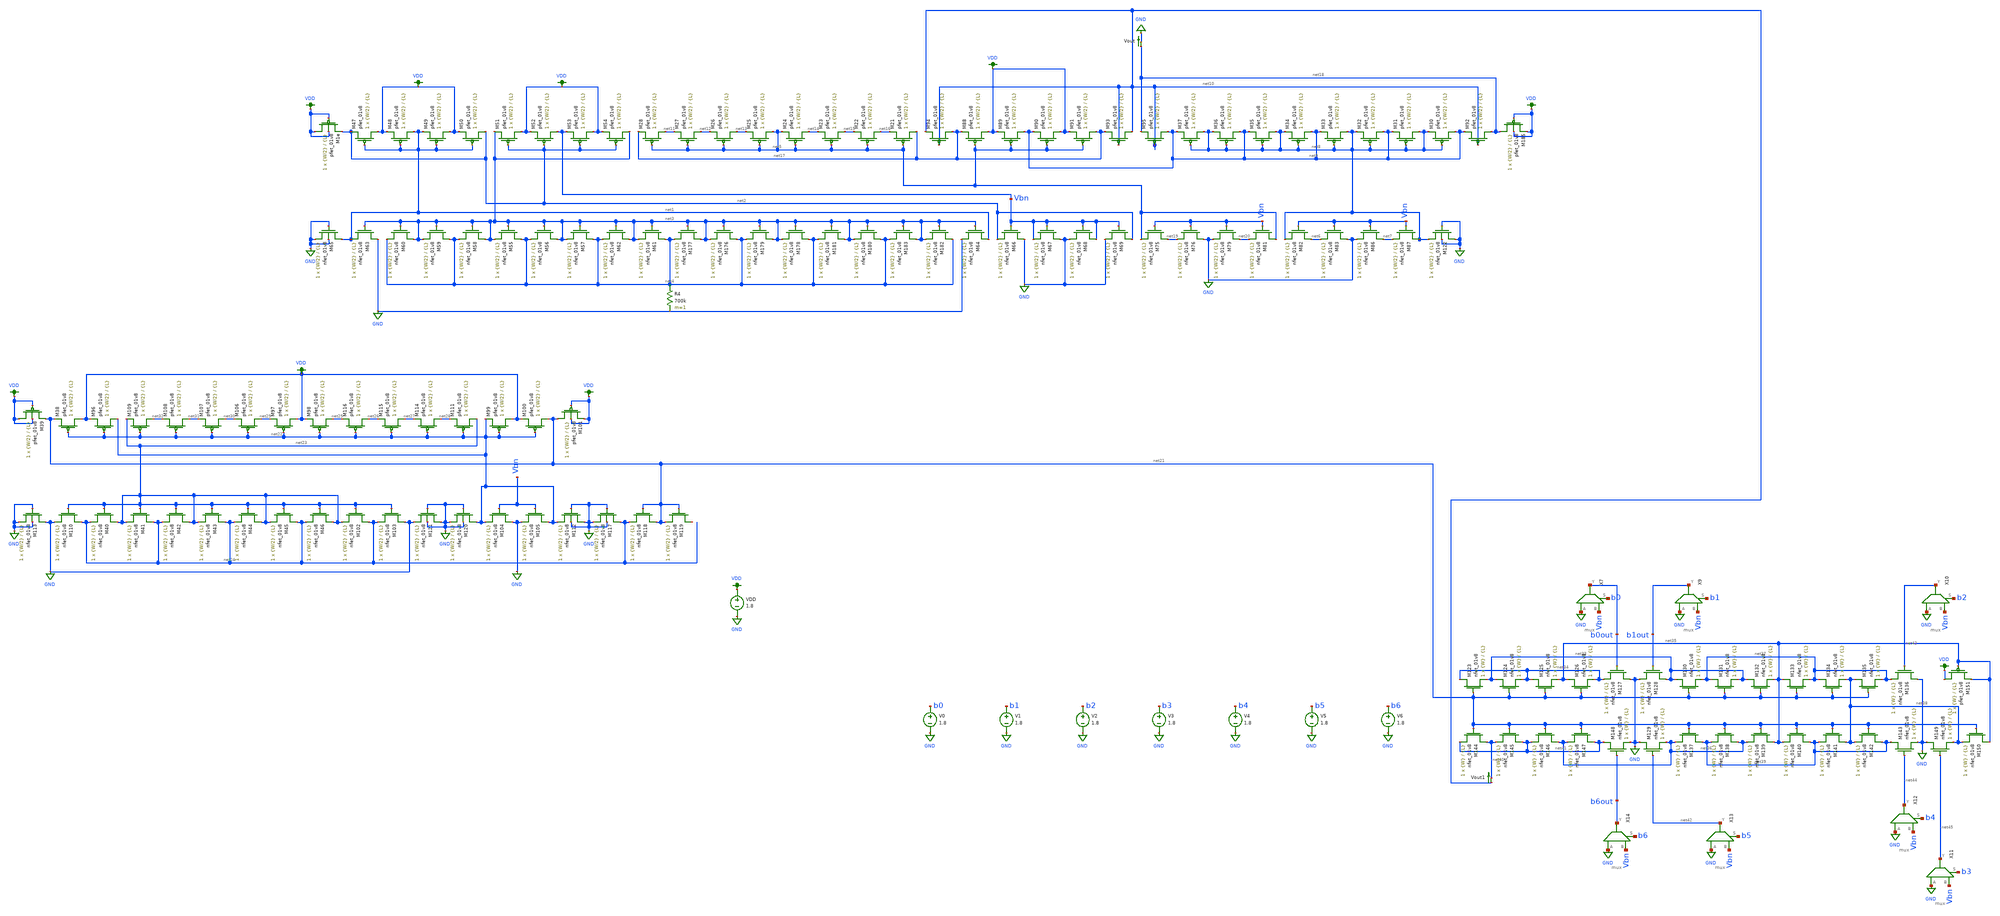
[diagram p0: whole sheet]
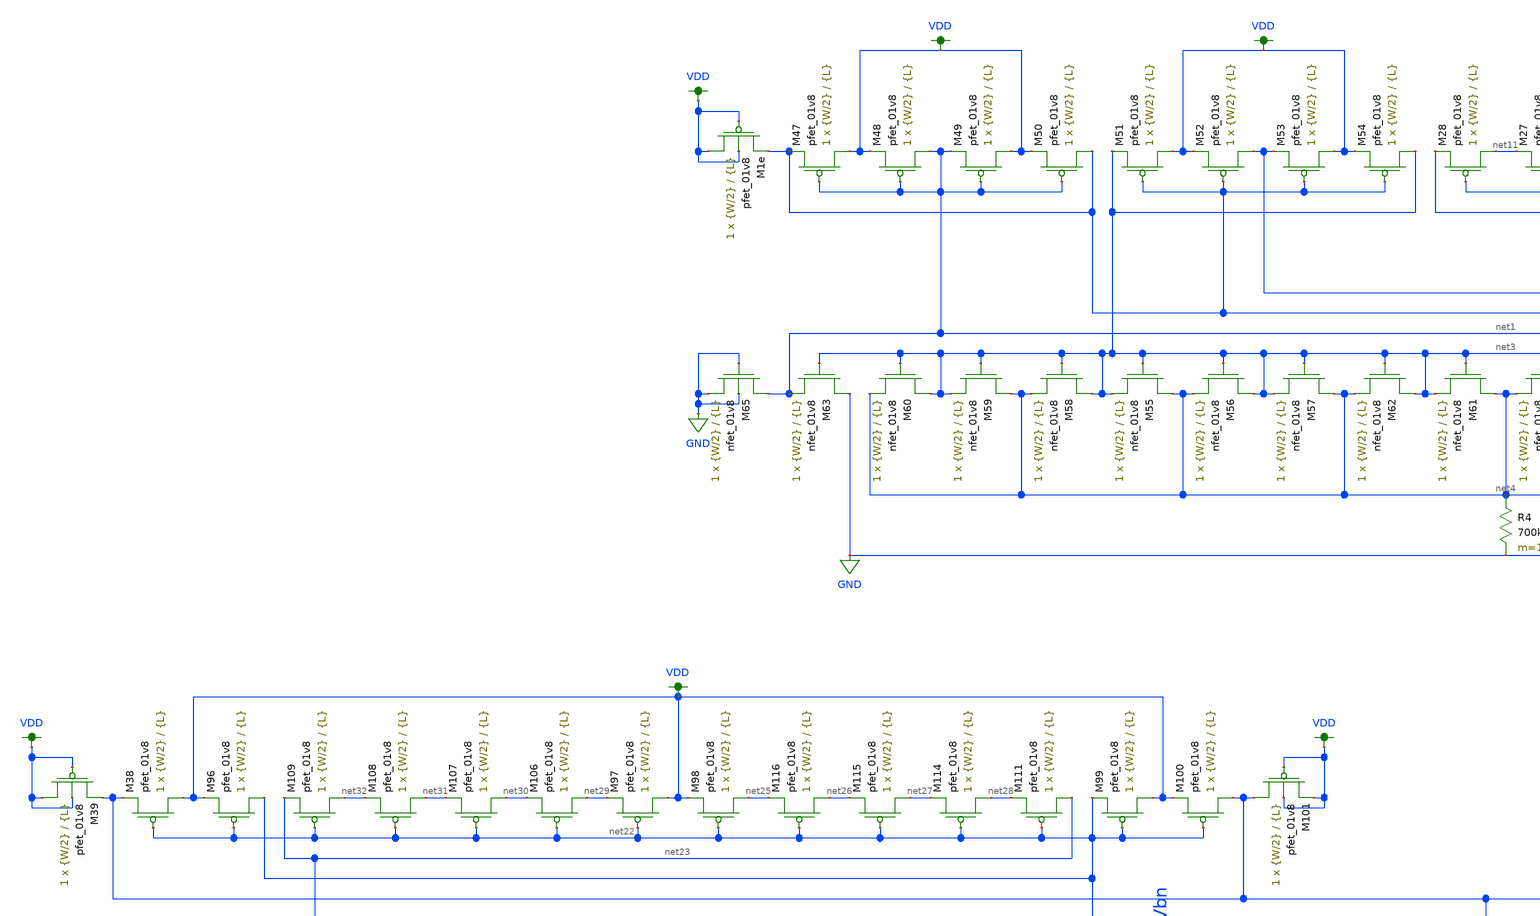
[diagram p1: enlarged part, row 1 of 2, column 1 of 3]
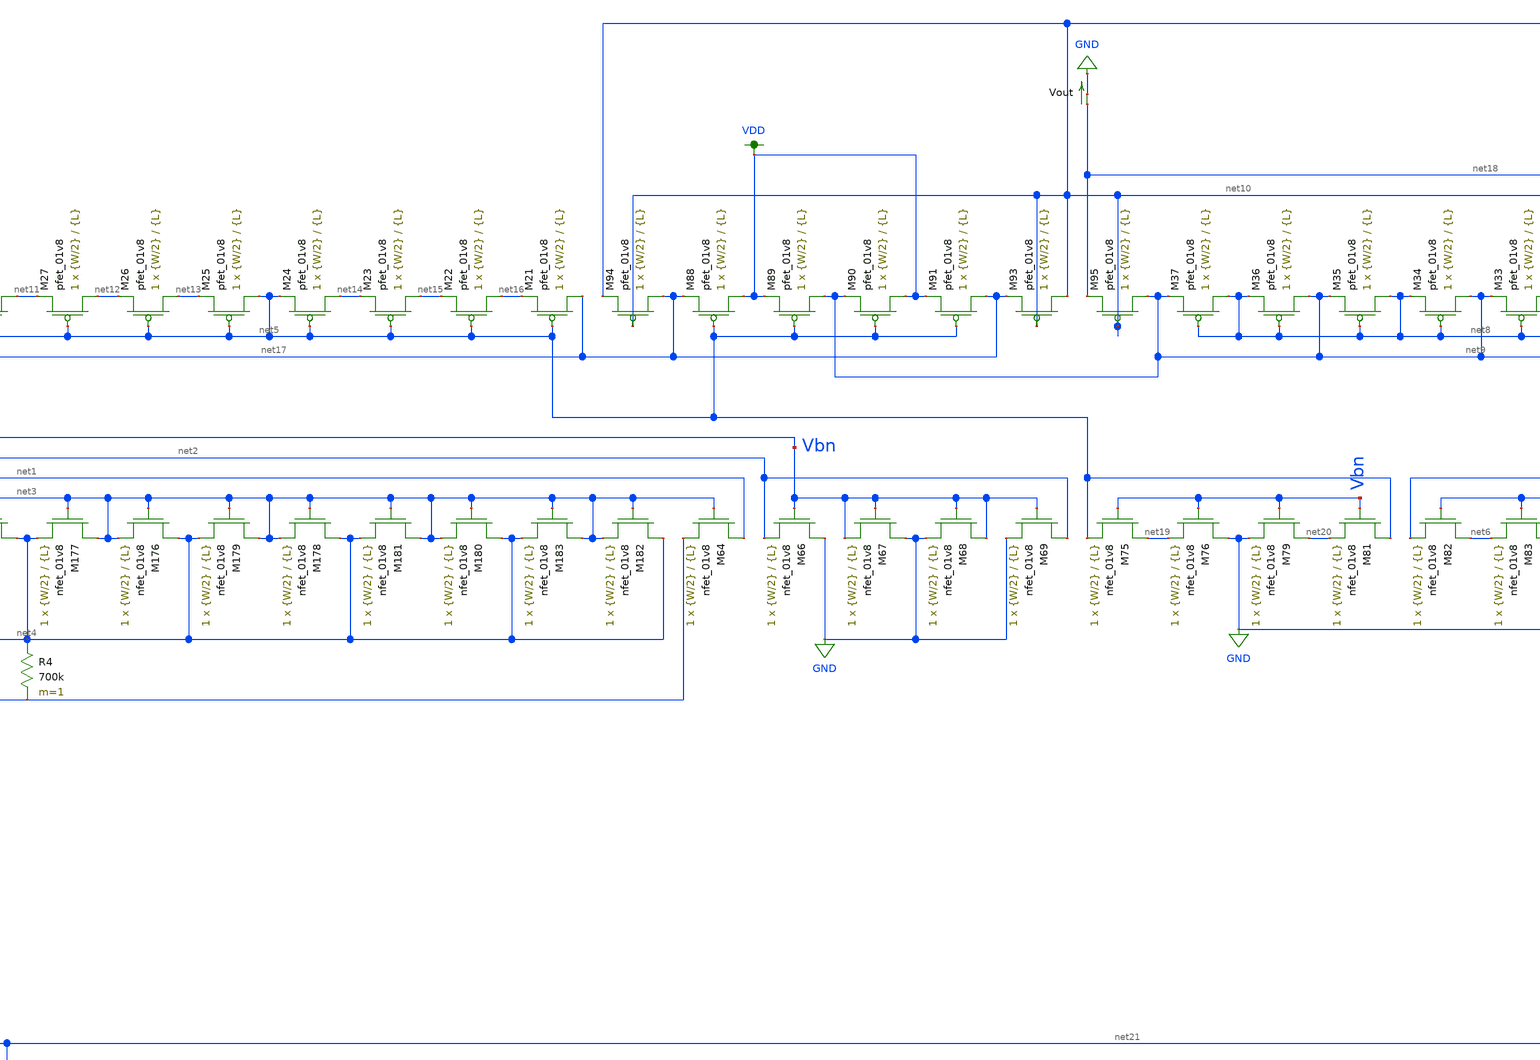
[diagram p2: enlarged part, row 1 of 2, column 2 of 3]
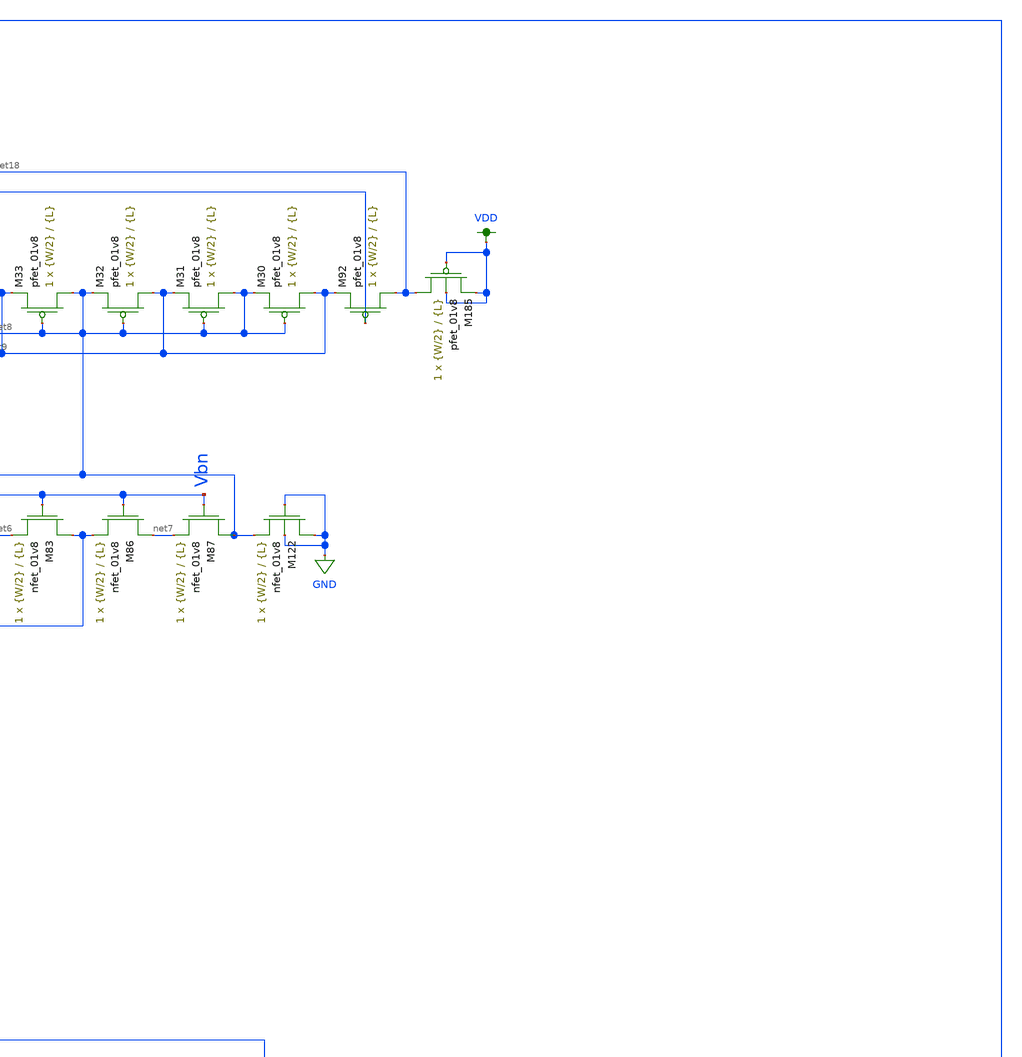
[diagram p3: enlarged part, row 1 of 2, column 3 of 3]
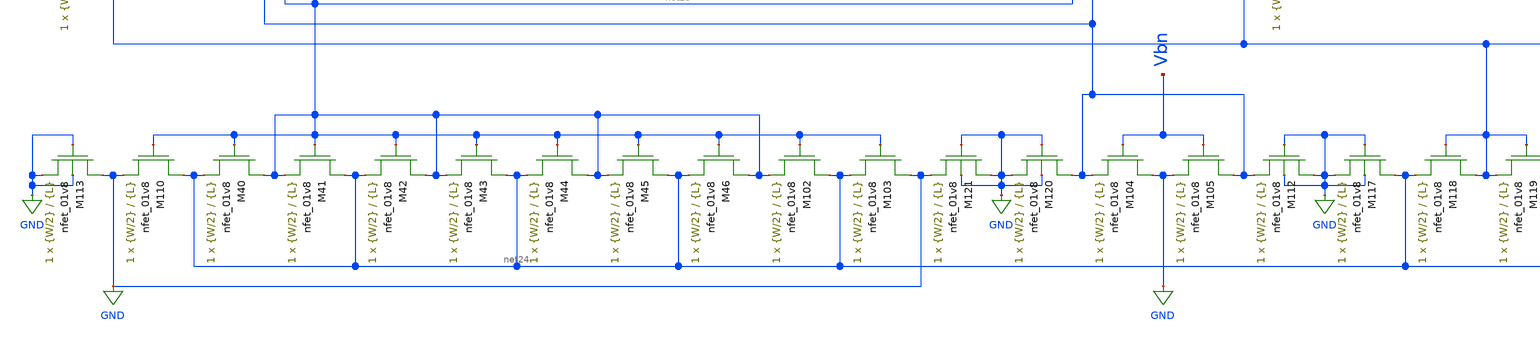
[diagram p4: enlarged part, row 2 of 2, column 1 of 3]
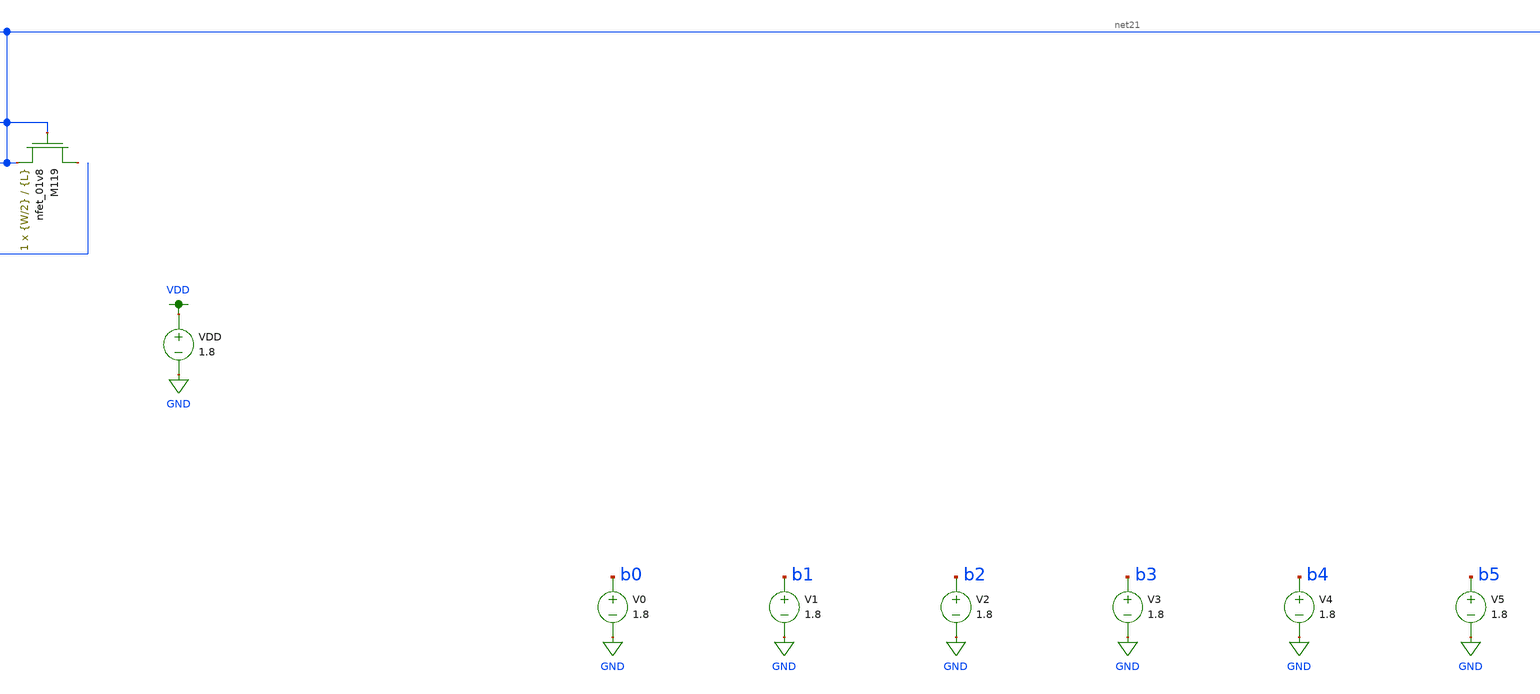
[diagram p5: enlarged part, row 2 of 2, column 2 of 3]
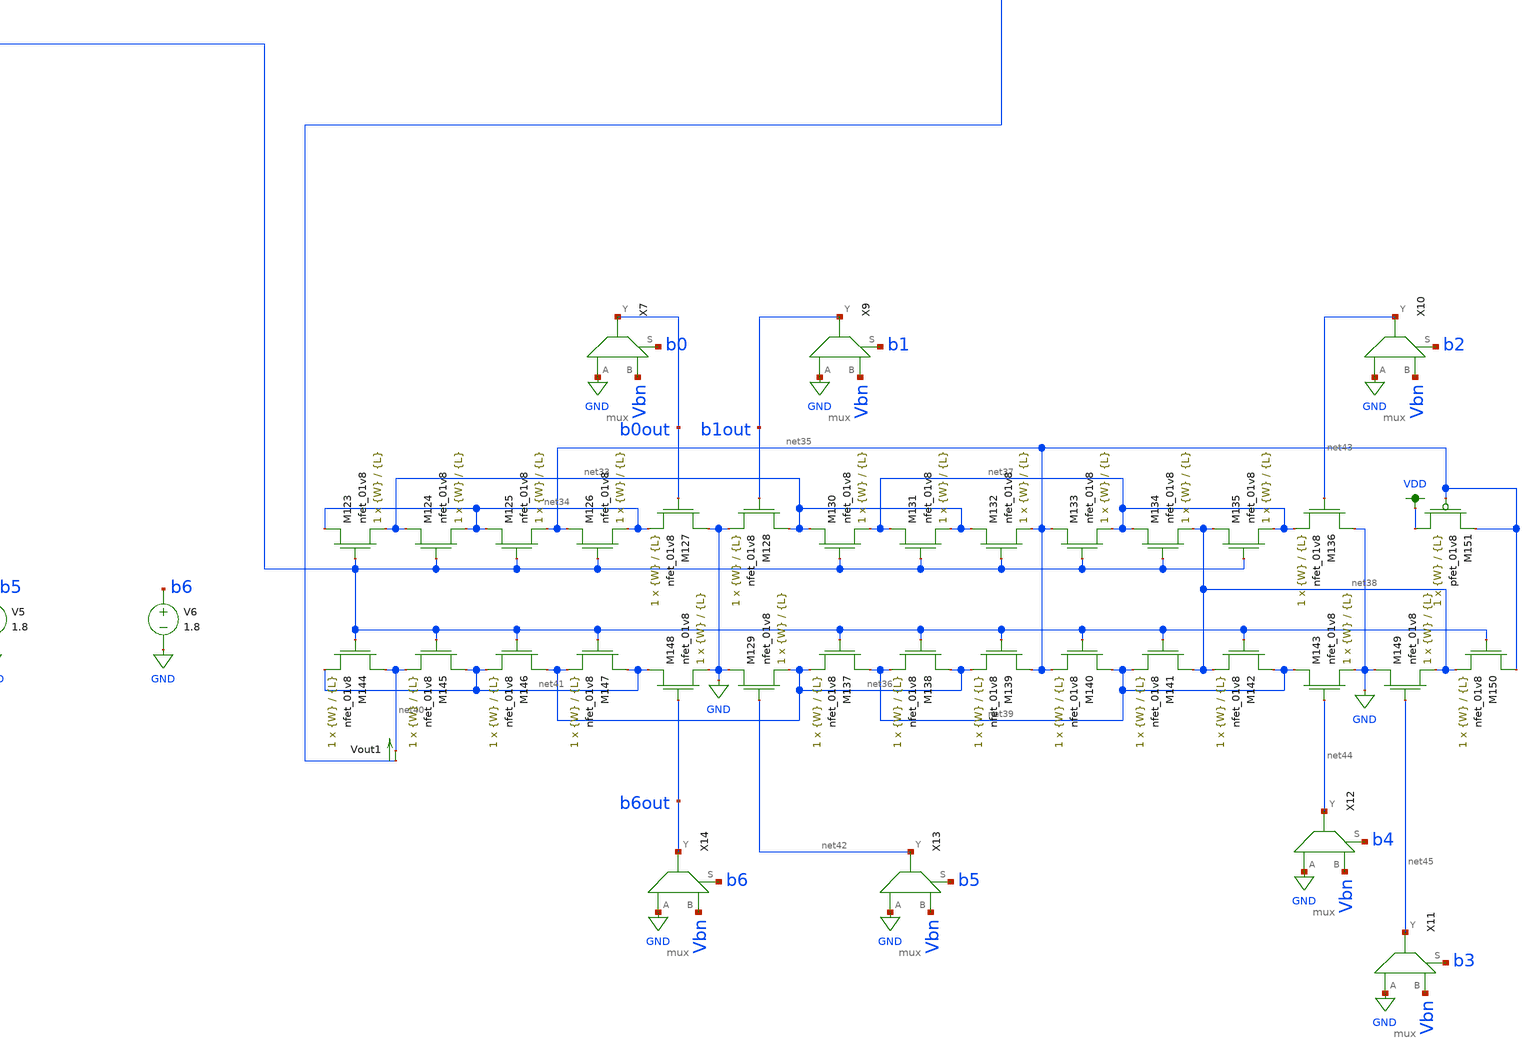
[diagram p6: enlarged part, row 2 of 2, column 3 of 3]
** sch_path: schematics/dac_dnl_inl_current_mirror_lds.sch
**.subckt dac_dnl_inl_current_mirror_lds
V0 b0 GND 1.8
V1 b1 GND 1.8
V2 b2 GND 1.8
V3 b3 GND 1.8
V4 b4 GND 1.8
V5 b5 GND 1.8
V6 b6 GND 1.8
VDD VDD GND 1.8
XM47 VDD net1 net2 VDD sky130_fd_pr__pfet_01v8 L={L} W={W/2} nf=1 ad='int((nf+1)/2) * W/nf * 0.29' as='int((nf+2)/2) * W/nf * 0.29'
+ pd='2*int((nf+1)/2) * (W/nf + 0.29)' ps='2*int((nf+2)/2) * (W/nf + 0.29)' nrd='0.29 / W' nrs='0.29 / W'
+ sa=0 sb=0 sd=0 mult=1 m=1
XM48 net1 net1 VDD VDD sky130_fd_pr__pfet_01v8 L={L} W={W/2} nf=1 ad='int((nf+1)/2) * W/nf * 0.29' as='int((nf+2)/2) * W/nf * 0.29'
+ pd='2*int((nf+1)/2) * (W/nf + 0.29)' ps='2*int((nf+2)/2) * (W/nf + 0.29)' nrd='0.29 / W' nrs='0.29 / W'
+ sa=0 sb=0 sd=0 mult=1 m=1
XM49 VDD net1 net1 VDD sky130_fd_pr__pfet_01v8 L={L} W={W/2} nf=1 ad='int((nf+1)/2) * W/nf * 0.29' as='int((nf+2)/2) * W/nf * 0.29'
+ pd='2*int((nf+1)/2) * (W/nf + 0.29)' ps='2*int((nf+2)/2) * (W/nf + 0.29)' nrd='0.29 / W' nrs='0.29 / W'
+ sa=0 sb=0 sd=0 mult=1 m=1
XM50 net2 net1 VDD VDD sky130_fd_pr__pfet_01v8 L={L} W={W/2} nf=1 ad='int((nf+1)/2) * W/nf * 0.29' as='int((nf+2)/2) * W/nf * 0.29'
+ pd='2*int((nf+1)/2) * (W/nf + 0.29)' ps='2*int((nf+2)/2) * (W/nf + 0.29)' nrd='0.29 / W' nrs='0.29 / W'
+ sa=0 sb=0 sd=0 mult=1 m=1
XM51 VDD net2 net3 VDD sky130_fd_pr__pfet_01v8 L={L} W={W/2} nf=1 ad='int((nf+1)/2) * W/nf * 0.29' as='int((nf+2)/2) * W/nf * 0.29'
+ pd='2*int((nf+1)/2) * (W/nf + 0.29)' ps='2*int((nf+2)/2) * (W/nf + 0.29)' nrd='0.29 / W' nrs='0.29 / W'
+ sa=0 sb=0 sd=0 mult=1 m=1
XM52 Vbn net2 VDD VDD sky130_fd_pr__pfet_01v8 L={L} W={W/2} nf=1 ad='int((nf+1)/2) * W/nf * 0.29' as='int((nf+2)/2) * W/nf * 0.29'
+ pd='2*int((nf+1)/2) * (W/nf + 0.29)' ps='2*int((nf+2)/2) * (W/nf + 0.29)' nrd='0.29 / W' nrs='0.29 / W'
+ sa=0 sb=0 sd=0 mult=1 m=1
XM53 VDD net2 Vbn VDD sky130_fd_pr__pfet_01v8 L={L} W={W/2} nf=1 ad='int((nf+1)/2) * W/nf * 0.29' as='int((nf+2)/2) * W/nf * 0.29'
+ pd='2*int((nf+1)/2) * (W/nf + 0.29)' ps='2*int((nf+2)/2) * (W/nf + 0.29)' nrd='0.29 / W' nrs='0.29 / W'
+ sa=0 sb=0 sd=0 mult=1 m=1
XM54 net3 net2 VDD VDD sky130_fd_pr__pfet_01v8 L={L} W={W/2} nf=1 ad='int((nf+1)/2) * W/nf * 0.29' as='int((nf+2)/2) * W/nf * 0.29'
+ pd='2*int((nf+1)/2) * (W/nf + 0.29)' ps='2*int((nf+2)/2) * (W/nf + 0.29)' nrd='0.29 / W' nrs='0.29 / W'
+ sa=0 sb=0 sd=0 mult=1 m=1
XM55 net4 net3 net3 GND sky130_fd_pr__nfet_01v8 L={L} W={W/2} nf=1 ad='int((nf+1)/2) * W/nf * 0.29' as='int((nf+2)/2) * W/nf * 0.29'
+ pd='2*int((nf+1)/2) * (W/nf + 0.29)' ps='2*int((nf+2)/2) * (W/nf + 0.29)' nrd='0.29 / W' nrs='0.29 / W'
+ sa=0 sb=0 sd=0 mult=1 m=1
XM56 net3 net3 net4 GND sky130_fd_pr__nfet_01v8 L={L} W={W/2} nf=1 ad='int((nf+1)/2) * W/nf * 0.29' as='int((nf+2)/2) * W/nf * 0.29'
+ pd='2*int((nf+1)/2) * (W/nf + 0.29)' ps='2*int((nf+2)/2) * (W/nf + 0.29)' nrd='0.29 / W' nrs='0.29 / W'
+ sa=0 sb=0 sd=0 mult=1 m=1
XM57 net4 net3 net3 GND sky130_fd_pr__nfet_01v8 L={L} W={W/2} nf=1 ad='int((nf+1)/2) * W/nf * 0.29' as='int((nf+2)/2) * W/nf * 0.29'
+ pd='2*int((nf+1)/2) * (W/nf + 0.29)' ps='2*int((nf+2)/2) * (W/nf + 0.29)' nrd='0.29 / W' nrs='0.29 / W'
+ sa=0 sb=0 sd=0 mult=1 m=1
XM58 net3 net3 net4 GND sky130_fd_pr__nfet_01v8 L={L} W={W/2} nf=1 ad='int((nf+1)/2) * W/nf * 0.29' as='int((nf+2)/2) * W/nf * 0.29'
+ pd='2*int((nf+1)/2) * (W/nf + 0.29)' ps='2*int((nf+2)/2) * (W/nf + 0.29)' nrd='0.29 / W' nrs='0.29 / W'
+ sa=0 sb=0 sd=0 mult=1 m=1
XM59 net4 net3 net3 GND sky130_fd_pr__nfet_01v8 L={L} W={W/2} nf=1 ad='int((nf+1)/2) * W/nf * 0.29' as='int((nf+2)/2) * W/nf * 0.29'
+ pd='2*int((nf+1)/2) * (W/nf + 0.29)' ps='2*int((nf+2)/2) * (W/nf + 0.29)' nrd='0.29 / W' nrs='0.29 / W'
+ sa=0 sb=0 sd=0 mult=1 m=1
XM60 net3 net3 net4 GND sky130_fd_pr__nfet_01v8 L={L} W={W/2} nf=1 ad='int((nf+1)/2) * W/nf * 0.29' as='int((nf+2)/2) * W/nf * 0.29'
+ pd='2*int((nf+1)/2) * (W/nf + 0.29)' ps='2*int((nf+2)/2) * (W/nf + 0.29)' nrd='0.29 / W' nrs='0.29 / W'
+ sa=0 sb=0 sd=0 mult=1 m=1
XM61 net4 net3 net3 GND sky130_fd_pr__nfet_01v8 L={L} W={W/2} nf=1 ad='int((nf+1)/2) * W/nf * 0.29' as='int((nf+2)/2) * W/nf * 0.29'
+ pd='2*int((nf+1)/2) * (W/nf + 0.29)' ps='2*int((nf+2)/2) * (W/nf + 0.29)' nrd='0.29 / W' nrs='0.29 / W'
+ sa=0 sb=0 sd=0 mult=1 m=1
XM62 net3 net3 net4 GND sky130_fd_pr__nfet_01v8 L={L} W={W/2} nf=1 ad='int((nf+1)/2) * W/nf * 0.29' as='int((nf+2)/2) * W/nf * 0.29'
+ pd='2*int((nf+1)/2) * (W/nf + 0.29)' ps='2*int((nf+2)/2) * (W/nf + 0.29)' nrd='0.29 / W' nrs='0.29 / W'
+ sa=0 sb=0 sd=0 mult=1 m=1
XM63 GND net3 net1 GND sky130_fd_pr__nfet_01v8 L={L} W={W/2} nf=1 ad='int((nf+1)/2) * W/nf * 0.29' as='int((nf+2)/2) * W/nf * 0.29'
+ pd='2*int((nf+1)/2) * (W/nf + 0.29)' ps='2*int((nf+2)/2) * (W/nf + 0.29)' nrd='0.29 / W' nrs='0.29 / W'
+ sa=0 sb=0 sd=0 mult=1 m=1
XM64 net1 net3 GND GND sky130_fd_pr__nfet_01v8 L={L} W={W/2} nf=1 ad='int((nf+1)/2) * W/nf * 0.29' as='int((nf+2)/2) * W/nf * 0.29'
+ pd='2*int((nf+1)/2) * (W/nf + 0.29)' ps='2*int((nf+2)/2) * (W/nf + 0.29)' nrd='0.29 / W' nrs='0.29 / W'
+ sa=0 sb=0 sd=0 mult=1 m=1
R4 net4 GND 700k m=1
XM1e VDD VDD net2 VDD sky130_fd_pr__pfet_01v8 L={L} W={W/2} nf=1 ad='int((nf+1)/2) * W/nf * 0.29' as='int((nf+2)/2) * W/nf * 0.29'
+ pd='2*int((nf+1)/2) * (W/nf + 0.29)' ps='2*int((nf+2)/2) * (W/nf + 0.29)' nrd='0.29 / W' nrs='0.29 / W'
+ sa=0 sb=0 sd=0 mult=1 m=1
XM65 net1 GND GND GND sky130_fd_pr__nfet_01v8 L={L} W={W/2} nf=1 ad='int((nf+1)/2) * W/nf * 0.29' as='int((nf+2)/2) * W/nf * 0.29'
+ pd='2*int((nf+1)/2) * (W/nf + 0.29)' ps='2*int((nf+2)/2) * (W/nf + 0.29)' nrd='0.29 / W' nrs='0.29 / W'
+ sa=0 sb=0 sd=0 mult=1 m=1
XM66 GND Vbn net2 GND sky130_fd_pr__nfet_01v8 L={L} W={W/2} nf=1 ad='int((nf+1)/2) * W/nf * 0.29' as='int((nf+2)/2) * W/nf * 0.29'
+ pd='2*int((nf+1)/2) * (W/nf + 0.29)' ps='2*int((nf+2)/2) * (W/nf + 0.29)' nrd='0.29 / W' nrs='0.29 / W'
+ sa=0 sb=0 sd=0 mult=1 m=1
XM67 GND Vbn Vbn GND sky130_fd_pr__nfet_01v8 L={L} W={W/2} nf=1 ad='int((nf+1)/2) * W/nf * 0.29' as='int((nf+2)/2) * W/nf * 0.29'
+ pd='2*int((nf+1)/2) * (W/nf + 0.29)' ps='2*int((nf+2)/2) * (W/nf + 0.29)' nrd='0.29 / W' nrs='0.29 / W'
+ sa=0 sb=0 sd=0 mult=1 m=1
XM68 Vbn Vbn GND GND sky130_fd_pr__nfet_01v8 L={L} W={W/2} nf=1 ad='int((nf+1)/2) * W/nf * 0.29' as='int((nf+2)/2) * W/nf * 0.29'
+ pd='2*int((nf+1)/2) * (W/nf + 0.29)' ps='2*int((nf+2)/2) * (W/nf + 0.29)' nrd='0.29 / W' nrs='0.29 / W'
+ sa=0 sb=0 sd=0 mult=1 m=1
XM69 net2 Vbn GND GND sky130_fd_pr__nfet_01v8 L={L} W={W/2} nf=1 ad='int((nf+1)/2) * W/nf * 0.29' as='int((nf+2)/2) * W/nf * 0.29'
+ pd='2*int((nf+1)/2) * (W/nf + 0.29)' ps='2*int((nf+2)/2) * (W/nf + 0.29)' nrd='0.29 / W' nrs='0.29 / W'
+ sa=0 sb=0 sd=0 mult=1 m=1
XM75 net19 Vbn net5 GND sky130_fd_pr__nfet_01v8 L={L} W={W/2} nf=1 ad='int((nf+1)/2) * W/nf * 0.29' as='int((nf+2)/2) * W/nf * 0.29'
+ pd='2*int((nf+1)/2) * (W/nf + 0.29)' ps='2*int((nf+2)/2) * (W/nf + 0.29)' nrd='0.29 / W' nrs='0.29 / W'
+ sa=0 sb=0 sd=0 mult=1 m=1
XM76 GND Vbn net19 GND sky130_fd_pr__nfet_01v8 L={L} W={W/2} nf=1 ad='int((nf+1)/2) * W/nf * 0.29' as='int((nf+2)/2) * W/nf * 0.29'
+ pd='2*int((nf+1)/2) * (W/nf + 0.29)' ps='2*int((nf+2)/2) * (W/nf + 0.29)' nrd='0.29 / W' nrs='0.29 / W'
+ sa=0 sb=0 sd=0 mult=1 m=1
XM79 net20 Vbn GND GND sky130_fd_pr__nfet_01v8 L={L} W={W/2} nf=1 ad='int((nf+1)/2) * W/nf * 0.29' as='int((nf+2)/2) * W/nf * 0.29'
+ pd='2*int((nf+1)/2) * (W/nf + 0.29)' ps='2*int((nf+2)/2) * (W/nf + 0.29)' nrd='0.29 / W' nrs='0.29 / W'
+ sa=0 sb=0 sd=0 mult=1 m=1
XM81 net5 Vbn net20 GND sky130_fd_pr__nfet_01v8 L={L} W={W/2} nf=1 ad='int((nf+1)/2) * W/nf * 0.29' as='int((nf+2)/2) * W/nf * 0.29'
+ pd='2*int((nf+1)/2) * (W/nf + 0.29)' ps='2*int((nf+2)/2) * (W/nf + 0.29)' nrd='0.29 / W' nrs='0.29 / W'
+ sa=0 sb=0 sd=0 mult=1 m=1
XM82 net6 Vbn net8 GND sky130_fd_pr__nfet_01v8 L={L} W={W/2} nf=1 ad='int((nf+1)/2) * W/nf * 0.29' as='int((nf+2)/2) * W/nf * 0.29'
+ pd='2*int((nf+1)/2) * (W/nf + 0.29)' ps='2*int((nf+2)/2) * (W/nf + 0.29)' nrd='0.29 / W' nrs='0.29 / W'
+ sa=0 sb=0 sd=0 mult=1 m=1
XM83 GND Vbn net6 GND sky130_fd_pr__nfet_01v8 L={L} W={W/2} nf=1 ad='int((nf+1)/2) * W/nf * 0.29' as='int((nf+2)/2) * W/nf * 0.29'
+ pd='2*int((nf+1)/2) * (W/nf + 0.29)' ps='2*int((nf+2)/2) * (W/nf + 0.29)' nrd='0.29 / W' nrs='0.29 / W'
+ sa=0 sb=0 sd=0 mult=1 m=1
XM86 net7 Vbn GND GND sky130_fd_pr__nfet_01v8 L={L} W={W/2} nf=1 ad='int((nf+1)/2) * W/nf * 0.29' as='int((nf+2)/2) * W/nf * 0.29'
+ pd='2*int((nf+1)/2) * (W/nf + 0.29)' ps='2*int((nf+2)/2) * (W/nf + 0.29)' nrd='0.29 / W' nrs='0.29 / W'
+ sa=0 sb=0 sd=0 mult=1 m=1
XM87 net8 Vbn net7 GND sky130_fd_pr__nfet_01v8 L={L} W={W/2} nf=1 ad='int((nf+1)/2) * W/nf * 0.29' as='int((nf+2)/2) * W/nf * 0.29'
+ pd='2*int((nf+1)/2) * (W/nf + 0.29)' ps='2*int((nf+2)/2) * (W/nf + 0.29)' nrd='0.29 / W' nrs='0.29 / W'
+ sa=0 sb=0 sd=0 mult=1 m=1
XM88 VDD net5 net17 VDD sky130_fd_pr__pfet_01v8 L={L} W={W/2} nf=1 ad='int((nf+1)/2) * W/nf * 0.29' as='int((nf+2)/2) * W/nf * 0.29'
+ pd='2*int((nf+1)/2) * (W/nf + 0.29)' ps='2*int((nf+2)/2) * (W/nf + 0.29)' nrd='0.29 / W' nrs='0.29 / W'
+ sa=0 sb=0 sd=0 mult=1 m=1
XM89 net9 net5 VDD VDD sky130_fd_pr__pfet_01v8 L={L} W={W/2} nf=1 ad='int((nf+1)/2) * W/nf * 0.29' as='int((nf+2)/2) * W/nf * 0.29'
+ pd='2*int((nf+1)/2) * (W/nf + 0.29)' ps='2*int((nf+2)/2) * (W/nf + 0.29)' nrd='0.29 / W' nrs='0.29 / W'
+ sa=0 sb=0 sd=0 mult=1 m=1
XM90 VDD net5 net9 VDD sky130_fd_pr__pfet_01v8 L={L} W={W/2} nf=1 ad='int((nf+1)/2) * W/nf * 0.29' as='int((nf+2)/2) * W/nf * 0.29'
+ pd='2*int((nf+1)/2) * (W/nf + 0.29)' ps='2*int((nf+2)/2) * (W/nf + 0.29)' nrd='0.29 / W' nrs='0.29 / W'
+ sa=0 sb=0 sd=0 mult=1 m=1
XM91 net17 net5 VDD VDD sky130_fd_pr__pfet_01v8 L={L} W={W/2} nf=1 ad='int((nf+1)/2) * W/nf * 0.29' as='int((nf+2)/2) * W/nf * 0.29'
+ pd='2*int((nf+1)/2) * (W/nf + 0.29)' ps='2*int((nf+2)/2) * (W/nf + 0.29)' nrd='0.29 / W' nrs='0.29 / W'
+ sa=0 sb=0 sd=0 mult=1 m=1
XM92 net18 net10 net9 VDD sky130_fd_pr__pfet_01v8 L={L} W={W/2} nf=1 ad='int((nf+1)/2) * W/nf * 0.29'
+ as='int((nf+2)/2) * W/nf * 0.29' pd='2*int((nf+1)/2) * (W/nf + 0.29)' ps='2*int((nf+2)/2) * (W/nf + 0.29)'
+ nrd='0.29 / W' nrs='0.29 / W' sa=0 sb=0 sd=0 mult=1 m=1
XM93 net10 net10 net17 VDD sky130_fd_pr__pfet_01v8 L={L} W={W/2} nf=1 ad='int((nf+1)/2) * W/nf * 0.29'
+ as='int((nf+2)/2) * W/nf * 0.29' pd='2*int((nf+1)/2) * (W/nf + 0.29)' ps='2*int((nf+2)/2) * (W/nf + 0.29)'
+ nrd='0.29 / W' nrs='0.29 / W' sa=0 sb=0 sd=0 mult=1 m=1
XM94 net17 net10 net10 VDD sky130_fd_pr__pfet_01v8 L={L} W={W/2} nf=1 ad='int((nf+1)/2) * W/nf * 0.29'
+ as='int((nf+2)/2) * W/nf * 0.29' pd='2*int((nf+1)/2) * (W/nf + 0.29)' ps='2*int((nf+2)/2) * (W/nf + 0.29)'
+ nrd='0.29 / W' nrs='0.29 / W' sa=0 sb=0 sd=0 mult=1 m=1
XM95 net9 net10 net18 VDD sky130_fd_pr__pfet_01v8 L={L} W={W/2} nf=1 ad='int((nf+1)/2) * W/nf * 0.29'
+ as='int((nf+2)/2) * W/nf * 0.29' pd='2*int((nf+1)/2) * (W/nf + 0.29)' ps='2*int((nf+2)/2) * (W/nf + 0.29)'
+ nrd='0.29 / W' nrs='0.29 / W' sa=0 sb=0 sd=0 mult=1 m=1
XM176 net4 net3 net3 GND sky130_fd_pr__nfet_01v8 L={L} W={W/2} nf=1 ad='int((nf+1)/2) * W/nf * 0.29'
+ as='int((nf+2)/2) * W/nf * 0.29' pd='2*int((nf+1)/2) * (W/nf + 0.29)' ps='2*int((nf+2)/2) * (W/nf + 0.29)'
+ nrd='0.29 / W' nrs='0.29 / W' sa=0 sb=0 sd=0 mult=1 m=1
XM177 net3 net3 net4 GND sky130_fd_pr__nfet_01v8 L={L} W={W/2} nf=1 ad='int((nf+1)/2) * W/nf * 0.29'
+ as='int((nf+2)/2) * W/nf * 0.29' pd='2*int((nf+1)/2) * (W/nf + 0.29)' ps='2*int((nf+2)/2) * (W/nf + 0.29)'
+ nrd='0.29 / W' nrs='0.29 / W' sa=0 sb=0 sd=0 mult=1 m=1
XM178 net4 net3 net3 GND sky130_fd_pr__nfet_01v8 L={L} W={W/2} nf=1 ad='int((nf+1)/2) * W/nf * 0.29'
+ as='int((nf+2)/2) * W/nf * 0.29' pd='2*int((nf+1)/2) * (W/nf + 0.29)' ps='2*int((nf+2)/2) * (W/nf + 0.29)'
+ nrd='0.29 / W' nrs='0.29 / W' sa=0 sb=0 sd=0 mult=1 m=1
XM179 net3 net3 net4 GND sky130_fd_pr__nfet_01v8 L={L} W={W/2} nf=1 ad='int((nf+1)/2) * W/nf * 0.29'
+ as='int((nf+2)/2) * W/nf * 0.29' pd='2*int((nf+1)/2) * (W/nf + 0.29)' ps='2*int((nf+2)/2) * (W/nf + 0.29)'
+ nrd='0.29 / W' nrs='0.29 / W' sa=0 sb=0 sd=0 mult=1 m=1
XM180 net4 net3 net3 GND sky130_fd_pr__nfet_01v8 L={L} W={W/2} nf=1 ad='int((nf+1)/2) * W/nf * 0.29'
+ as='int((nf+2)/2) * W/nf * 0.29' pd='2*int((nf+1)/2) * (W/nf + 0.29)' ps='2*int((nf+2)/2) * (W/nf + 0.29)'
+ nrd='0.29 / W' nrs='0.29 / W' sa=0 sb=0 sd=0 mult=1 m=1
XM181 net3 net3 net4 GND sky130_fd_pr__nfet_01v8 L={L} W={W/2} nf=1 ad='int((nf+1)/2) * W/nf * 0.29'
+ as='int((nf+2)/2) * W/nf * 0.29' pd='2*int((nf+1)/2) * (W/nf + 0.29)' ps='2*int((nf+2)/2) * (W/nf + 0.29)'
+ nrd='0.29 / W' nrs='0.29 / W' sa=0 sb=0 sd=0 mult=1 m=1
XM182 net4 net3 net3 GND sky130_fd_pr__nfet_01v8 L={L} W={W/2} nf=1 ad='int((nf+1)/2) * W/nf * 0.29'
+ as='int((nf+2)/2) * W/nf * 0.29' pd='2*int((nf+1)/2) * (W/nf + 0.29)' ps='2*int((nf+2)/2) * (W/nf + 0.29)'
+ nrd='0.29 / W' nrs='0.29 / W' sa=0 sb=0 sd=0 mult=1 m=1
XM183 net3 net3 net4 GND sky130_fd_pr__nfet_01v8 L={L} W={W/2} nf=1 ad='int((nf+1)/2) * W/nf * 0.29'
+ as='int((nf+2)/2) * W/nf * 0.29' pd='2*int((nf+1)/2) * (W/nf + 0.29)' ps='2*int((nf+2)/2) * (W/nf + 0.29)'
+ nrd='0.29 / W' nrs='0.29 / W' sa=0 sb=0 sd=0 mult=1 m=1
XM185 net18 VDD VDD VDD sky130_fd_pr__pfet_01v8 L={L} W={W/2} nf=1 ad='int((nf+1)/2) * W/nf * 0.29' as='int((nf+2)/2) * W/nf * 0.29'
+ pd='2*int((nf+1)/2) * (W/nf + 0.29)' ps='2*int((nf+2)/2) * (W/nf + 0.29)' nrd='0.29 / W' nrs='0.29 / W'
+ sa=0 sb=0 sd=0 mult=1 m=1
Vout net18 GND 0
.save i(vout)
XM21 net17 net5 net16 VDD sky130_fd_pr__pfet_01v8 L={L} W={W/2} nf=1 ad='int((nf+1)/2) * W/nf * 0.29'
+ as='int((nf+2)/2) * W/nf * 0.29' pd='2*int((nf+1)/2) * (W/nf + 0.29)' ps='2*int((nf+2)/2) * (W/nf + 0.29)'
+ nrd='0.29 / W' nrs='0.29 / W' sa=0 sb=0 sd=0 mult=1 m=1
XM22 net16 net5 net15 VDD sky130_fd_pr__pfet_01v8 L={L} W={W/2} nf=1 ad='int((nf+1)/2) * W/nf * 0.29'
+ as='int((nf+2)/2) * W/nf * 0.29' pd='2*int((nf+1)/2) * (W/nf + 0.29)' ps='2*int((nf+2)/2) * (W/nf + 0.29)'
+ nrd='0.29 / W' nrs='0.29 / W' sa=0 sb=0 sd=0 mult=1 m=1
XM23 net15 net5 net14 VDD sky130_fd_pr__pfet_01v8 L={L} W={W/2} nf=1 ad='int((nf+1)/2) * W/nf * 0.29'
+ as='int((nf+2)/2) * W/nf * 0.29' pd='2*int((nf+1)/2) * (W/nf + 0.29)' ps='2*int((nf+2)/2) * (W/nf + 0.29)'
+ nrd='0.29 / W' nrs='0.29 / W' sa=0 sb=0 sd=0 mult=1 m=1
XM24 net14 net5 net5 VDD sky130_fd_pr__pfet_01v8 L={L} W={W/2} nf=1 ad='int((nf+1)/2) * W/nf * 0.29'
+ as='int((nf+2)/2) * W/nf * 0.29' pd='2*int((nf+1)/2) * (W/nf + 0.29)' ps='2*int((nf+2)/2) * (W/nf + 0.29)'
+ nrd='0.29 / W' nrs='0.29 / W' sa=0 sb=0 sd=0 mult=1 m=1
XM25 net5 net5 net13 VDD sky130_fd_pr__pfet_01v8 L={L} W={W/2} nf=1 ad='int((nf+1)/2) * W/nf * 0.29'
+ as='int((nf+2)/2) * W/nf * 0.29' pd='2*int((nf+1)/2) * (W/nf + 0.29)' ps='2*int((nf+2)/2) * (W/nf + 0.29)'
+ nrd='0.29 / W' nrs='0.29 / W' sa=0 sb=0 sd=0 mult=1 m=1
XM26 net13 net5 net12 VDD sky130_fd_pr__pfet_01v8 L={L} W={W/2} nf=1 ad='int((nf+1)/2) * W/nf * 0.29'
+ as='int((nf+2)/2) * W/nf * 0.29' pd='2*int((nf+1)/2) * (W/nf + 0.29)' ps='2*int((nf+2)/2) * (W/nf + 0.29)'
+ nrd='0.29 / W' nrs='0.29 / W' sa=0 sb=0 sd=0 mult=1 m=1
XM27 net12 net5 net11 VDD sky130_fd_pr__pfet_01v8 L={L} W={W/2} nf=1 ad='int((nf+1)/2) * W/nf * 0.29'
+ as='int((nf+2)/2) * W/nf * 0.29' pd='2*int((nf+1)/2) * (W/nf + 0.29)' ps='2*int((nf+2)/2) * (W/nf + 0.29)'
+ nrd='0.29 / W' nrs='0.29 / W' sa=0 sb=0 sd=0 mult=1 m=1
XM28 net11 net5 net17 VDD sky130_fd_pr__pfet_01v8 L={L} W={W/2} nf=1 ad='int((nf+1)/2) * W/nf * 0.29'
+ as='int((nf+2)/2) * W/nf * 0.29' pd='2*int((nf+1)/2) * (W/nf + 0.29)' ps='2*int((nf+2)/2) * (W/nf + 0.29)'
+ nrd='0.29 / W' nrs='0.29 / W' sa=0 sb=0 sd=0 mult=1 m=1
XM30 net9 net8 net8 VDD sky130_fd_pr__pfet_01v8 L={L} W={W/2} nf=1 ad='int((nf+1)/2) * W/nf * 0.29' as='int((nf+2)/2) * W/nf * 0.29'
+ pd='2*int((nf+1)/2) * (W/nf + 0.29)' ps='2*int((nf+2)/2) * (W/nf + 0.29)' nrd='0.29 / W' nrs='0.29 / W'
+ sa=0 sb=0 sd=0 mult=1 m=1
XM31 net8 net8 net9 VDD sky130_fd_pr__pfet_01v8 L={L} W={W/2} nf=1 ad='int((nf+1)/2) * W/nf * 0.29' as='int((nf+2)/2) * W/nf * 0.29'
+ pd='2*int((nf+1)/2) * (W/nf + 0.29)' ps='2*int((nf+2)/2) * (W/nf + 0.29)' nrd='0.29 / W' nrs='0.29 / W'
+ sa=0 sb=0 sd=0 mult=1 m=1
XM32 net9 net8 net8 VDD sky130_fd_pr__pfet_01v8 L={L} W={W/2} nf=1 ad='int((nf+1)/2) * W/nf * 0.29' as='int((nf+2)/2) * W/nf * 0.29'
+ pd='2*int((nf+1)/2) * (W/nf + 0.29)' ps='2*int((nf+2)/2) * (W/nf + 0.29)' nrd='0.29 / W' nrs='0.29 / W'
+ sa=0 sb=0 sd=0 mult=1 m=1
XM33 net8 net8 net9 VDD sky130_fd_pr__pfet_01v8 L={L} W={W/2} nf=1 ad='int((nf+1)/2) * W/nf * 0.29' as='int((nf+2)/2) * W/nf * 0.29'
+ pd='2*int((nf+1)/2) * (W/nf + 0.29)' ps='2*int((nf+2)/2) * (W/nf + 0.29)' nrd='0.29 / W' nrs='0.29 / W'
+ sa=0 sb=0 sd=0 mult=1 m=1
XM34 net9 net8 net8 VDD sky130_fd_pr__pfet_01v8 L={L} W={W/2} nf=1 ad='int((nf+1)/2) * W/nf * 0.29' as='int((nf+2)/2) * W/nf * 0.29'
+ pd='2*int((nf+1)/2) * (W/nf + 0.29)' ps='2*int((nf+2)/2) * (W/nf + 0.29)' nrd='0.29 / W' nrs='0.29 / W'
+ sa=0 sb=0 sd=0 mult=1 m=1
XM35 net8 net8 net9 VDD sky130_fd_pr__pfet_01v8 L={L} W={W/2} nf=1 ad='int((nf+1)/2) * W/nf * 0.29' as='int((nf+2)/2) * W/nf * 0.29'
+ pd='2*int((nf+1)/2) * (W/nf + 0.29)' ps='2*int((nf+2)/2) * (W/nf + 0.29)' nrd='0.29 / W' nrs='0.29 / W'
+ sa=0 sb=0 sd=0 mult=1 m=1
XM36 net9 net8 net8 VDD sky130_fd_pr__pfet_01v8 L={L} W={W/2} nf=1 ad='int((nf+1)/2) * W/nf * 0.29' as='int((nf+2)/2) * W/nf * 0.29'
+ pd='2*int((nf+1)/2) * (W/nf + 0.29)' ps='2*int((nf+2)/2) * (W/nf + 0.29)' nrd='0.29 / W' nrs='0.29 / W'
+ sa=0 sb=0 sd=0 mult=1 m=1
XM37 net8 net8 net9 VDD sky130_fd_pr__pfet_01v8 L={L} W={W/2} nf=1 ad='int((nf+1)/2) * W/nf * 0.29' as='int((nf+2)/2) * W/nf * 0.29'
+ pd='2*int((nf+1)/2) * (W/nf + 0.29)' ps='2*int((nf+2)/2) * (W/nf + 0.29)' nrd='0.29 / W' nrs='0.29 / W'
+ sa=0 sb=0 sd=0 mult=1 m=1
XM38 VDD net22 net21 VDD sky130_fd_pr__pfet_01v8 L={L} W={W/2} nf=1 ad='int((nf+1)/2) * W/nf * 0.29'
+ as='int((nf+2)/2) * W/nf * 0.29' pd='2*int((nf+1)/2) * (W/nf + 0.29)' ps='2*int((nf+2)/2) * (W/nf + 0.29)'
+ nrd='0.29 / W' nrs='0.29 / W' sa=0 sb=0 sd=0 mult=1 m=1
XM39 VDD VDD net21 VDD sky130_fd_pr__pfet_01v8 L={L} W={W/2} nf=1 ad='int((nf+1)/2) * W/nf * 0.29' as='int((nf+2)/2) * W/nf * 0.29'
+ pd='2*int((nf+1)/2) * (W/nf + 0.29)' ps='2*int((nf+2)/2) * (W/nf + 0.29)' nrd='0.29 / W' nrs='0.29 / W'
+ sa=0 sb=0 sd=0 mult=1 m=1
XM96 net22 net22 VDD VDD sky130_fd_pr__pfet_01v8 L={L} W={W/2} nf=1 ad='int((nf+1)/2) * W/nf * 0.29'
+ as='int((nf+2)/2) * W/nf * 0.29' pd='2*int((nf+1)/2) * (W/nf + 0.29)' ps='2*int((nf+2)/2) * (W/nf + 0.29)'
+ nrd='0.29 / W' nrs='0.29 / W' sa=0 sb=0 sd=0 mult=1 m=1
XM97 VDD net22 net29 VDD sky130_fd_pr__pfet_01v8 L={L} W={W/2} nf=1 ad='int((nf+1)/2) * W/nf * 0.29'
+ as='int((nf+2)/2) * W/nf * 0.29' pd='2*int((nf+1)/2) * (W/nf + 0.29)' ps='2*int((nf+2)/2) * (W/nf + 0.29)'
+ nrd='0.29 / W' nrs='0.29 / W' sa=0 sb=0 sd=0 mult=1 m=1
XM98 net25 net22 VDD VDD sky130_fd_pr__pfet_01v8 L={L} W={W/2} nf=1 ad='int((nf+1)/2) * W/nf * 0.29'
+ as='int((nf+2)/2) * W/nf * 0.29' pd='2*int((nf+1)/2) * (W/nf + 0.29)' ps='2*int((nf+2)/2) * (W/nf + 0.29)'
+ nrd='0.29 / W' nrs='0.29 / W' sa=0 sb=0 sd=0 mult=1 m=1
XM99 VDD net22 net22 VDD sky130_fd_pr__pfet_01v8 L={L} W={W/2} nf=1 ad='int((nf+1)/2) * W/nf * 0.29'
+ as='int((nf+2)/2) * W/nf * 0.29' pd='2*int((nf+1)/2) * (W/nf + 0.29)' ps='2*int((nf+2)/2) * (W/nf + 0.29)'
+ nrd='0.29 / W' nrs='0.29 / W' sa=0 sb=0 sd=0 mult=1 m=1
XM100 net21 net22 VDD VDD sky130_fd_pr__pfet_01v8 L={L} W={W/2} nf=1 ad='int((nf+1)/2) * W/nf * 0.29'
+ as='int((nf+2)/2) * W/nf * 0.29' pd='2*int((nf+1)/2) * (W/nf + 0.29)' ps='2*int((nf+2)/2) * (W/nf + 0.29)'
+ nrd='0.29 / W' nrs='0.29 / W' sa=0 sb=0 sd=0 mult=1 m=1
XM101 net21 VDD VDD VDD sky130_fd_pr__pfet_01v8 L={L} W={W/2} nf=1 ad='int((nf+1)/2) * W/nf * 0.29' as='int((nf+2)/2) * W/nf * 0.29'
+ pd='2*int((nf+1)/2) * (W/nf + 0.29)' ps='2*int((nf+2)/2) * (W/nf + 0.29)' nrd='0.29 / W' nrs='0.29 / W'
+ sa=0 sb=0 sd=0 mult=1 m=1
XM110 net24 net23 GND GND sky130_fd_pr__nfet_01v8 L={L} W={W/2} nf=1 ad='int((nf+1)/2) * W/nf * 0.29'
+ as='int((nf+2)/2) * W/nf * 0.29' pd='2*int((nf+1)/2) * (W/nf + 0.29)' ps='2*int((nf+2)/2) * (W/nf + 0.29)'
+ nrd='0.29 / W' nrs='0.29 / W' sa=0 sb=0 sd=0 mult=1 m=1
XM112 GND GND net22 GND sky130_fd_pr__nfet_01v8 L={L} W={W/2} nf=1 ad='int((nf+1)/2) * W/nf * 0.29' as='int((nf+2)/2) * W/nf * 0.29'
+ pd='2*int((nf+1)/2) * (W/nf + 0.29)' ps='2*int((nf+2)/2) * (W/nf + 0.29)' nrd='0.29 / W' nrs='0.29 / W'
+ sa=0 sb=0 sd=0 mult=1 m=1
XM113 GND GND GND GND sky130_fd_pr__nfet_01v8 L={L} W={W/2} nf=1 ad='int((nf+1)/2) * W/nf * 0.29' as='int((nf+2)/2) * W/nf * 0.29'
+ pd='2*int((nf+1)/2) * (W/nf + 0.29)' ps='2*int((nf+2)/2) * (W/nf + 0.29)' nrd='0.29 / W' nrs='0.29 / W'
+ sa=0 sb=0 sd=0 mult=1 m=1
XM120 net22 GND GND GND sky130_fd_pr__nfet_01v8 L={L} W={W/2} nf=1 ad='int((nf+1)/2) * W/nf * 0.29' as='int((nf+2)/2) * W/nf * 0.29'
+ pd='2*int((nf+1)/2) * (W/nf + 0.29)' ps='2*int((nf+2)/2) * (W/nf + 0.29)' nrd='0.29 / W' nrs='0.29 / W'
+ sa=0 sb=0 sd=0 mult=1 m=1
XM121 GND GND GND GND sky130_fd_pr__nfet_01v8 L={L} W={W/2} nf=1 ad='int((nf+1)/2) * W/nf * 0.29' as='int((nf+2)/2) * W/nf * 0.29'
+ pd='2*int((nf+1)/2) * (W/nf + 0.29)' ps='2*int((nf+2)/2) * (W/nf + 0.29)' nrd='0.29 / W' nrs='0.29 / W'
+ sa=0 sb=0 sd=0 mult=1 m=1
XM40 net23 net23 net24 GND sky130_fd_pr__nfet_01v8 L={L} W={W/2} nf=1 ad='int((nf+1)/2) * W/nf * 0.29'
+ as='int((nf+2)/2) * W/nf * 0.29' pd='2*int((nf+1)/2) * (W/nf + 0.29)' ps='2*int((nf+2)/2) * (W/nf + 0.29)'
+ nrd='0.29 / W' nrs='0.29 / W' sa=0 sb=0 sd=0 mult=1 m=1
XM41 net24 net23 net23 GND sky130_fd_pr__nfet_01v8 L={L} W={W/2} nf=1 ad='int((nf+1)/2) * W/nf * 0.29'
+ as='int((nf+2)/2) * W/nf * 0.29' pd='2*int((nf+1)/2) * (W/nf + 0.29)' ps='2*int((nf+2)/2) * (W/nf + 0.29)'
+ nrd='0.29 / W' nrs='0.29 / W' sa=0 sb=0 sd=0 mult=1 m=1
XM42 net23 net23 net24 GND sky130_fd_pr__nfet_01v8 L={L} W={W/2} nf=1 ad='int((nf+1)/2) * W/nf * 0.29'
+ as='int((nf+2)/2) * W/nf * 0.29' pd='2*int((nf+1)/2) * (W/nf + 0.29)' ps='2*int((nf+2)/2) * (W/nf + 0.29)'
+ nrd='0.29 / W' nrs='0.29 / W' sa=0 sb=0 sd=0 mult=1 m=1
XM43 net24 net23 net23 GND sky130_fd_pr__nfet_01v8 L={L} W={W/2} nf=1 ad='int((nf+1)/2) * W/nf * 0.29'
+ as='int((nf+2)/2) * W/nf * 0.29' pd='2*int((nf+1)/2) * (W/nf + 0.29)' ps='2*int((nf+2)/2) * (W/nf + 0.29)'
+ nrd='0.29 / W' nrs='0.29 / W' sa=0 sb=0 sd=0 mult=1 m=1
XM44 net23 net23 net24 GND sky130_fd_pr__nfet_01v8 L={L} W={W/2} nf=1 ad='int((nf+1)/2) * W/nf * 0.29'
+ as='int((nf+2)/2) * W/nf * 0.29' pd='2*int((nf+1)/2) * (W/nf + 0.29)' ps='2*int((nf+2)/2) * (W/nf + 0.29)'
+ nrd='0.29 / W' nrs='0.29 / W' sa=0 sb=0 sd=0 mult=1 m=1
XM45 net24 net23 net23 GND sky130_fd_pr__nfet_01v8 L={L} W={W/2} nf=1 ad='int((nf+1)/2) * W/nf * 0.29'
+ as='int((nf+2)/2) * W/nf * 0.29' pd='2*int((nf+1)/2) * (W/nf + 0.29)' ps='2*int((nf+2)/2) * (W/nf + 0.29)'
+ nrd='0.29 / W' nrs='0.29 / W' sa=0 sb=0 sd=0 mult=1 m=1
XM46 net23 net23 net24 GND sky130_fd_pr__nfet_01v8 L={L} W={W/2} nf=1 ad='int((nf+1)/2) * W/nf * 0.29'
+ as='int((nf+2)/2) * W/nf * 0.29' pd='2*int((nf+1)/2) * (W/nf + 0.29)' ps='2*int((nf+2)/2) * (W/nf + 0.29)'
+ nrd='0.29 / W' nrs='0.29 / W' sa=0 sb=0 sd=0 mult=1 m=1
XM102 net24 net23 net23 GND sky130_fd_pr__nfet_01v8 L={L} W={W/2} nf=1 ad='int((nf+1)/2) * W/nf * 0.29'
+ as='int((nf+2)/2) * W/nf * 0.29' pd='2*int((nf+1)/2) * (W/nf + 0.29)' ps='2*int((nf+2)/2) * (W/nf + 0.29)'
+ nrd='0.29 / W' nrs='0.29 / W' sa=0 sb=0 sd=0 mult=1 m=1
XM103 GND net23 net24 GND sky130_fd_pr__nfet_01v8 L={L} W={W/2} nf=1 ad='int((nf+1)/2) * W/nf * 0.29'
+ as='int((nf+2)/2) * W/nf * 0.29' pd='2*int((nf+1)/2) * (W/nf + 0.29)' ps='2*int((nf+2)/2) * (W/nf + 0.29)'
+ nrd='0.29 / W' nrs='0.29 / W' sa=0 sb=0 sd=0 mult=1 m=1
XM104 GND Vbn net22 GND sky130_fd_pr__nfet_01v8 L={L} W={W/2} nf=1 ad='int((nf+1)/2) * W/nf * 0.29' as='int((nf+2)/2) * W/nf * 0.29'
+ pd='2*int((nf+1)/2) * (W/nf + 0.29)' ps='2*int((nf+2)/2) * (W/nf + 0.29)' nrd='0.29 / W' nrs='0.29 / W'
+ sa=0 sb=0 sd=0 mult=1 m=1
XM105 net22 Vbn GND GND sky130_fd_pr__nfet_01v8 L={L} W={W/2} nf=1 ad='int((nf+1)/2) * W/nf * 0.29' as='int((nf+2)/2) * W/nf * 0.29'
+ pd='2*int((nf+1)/2) * (W/nf + 0.29)' ps='2*int((nf+2)/2) * (W/nf + 0.29)' nrd='0.29 / W' nrs='0.29 / W'
+ sa=0 sb=0 sd=0 mult=1 m=1
XM106 net29 net22 net30 VDD sky130_fd_pr__pfet_01v8 L={L} W={W/2} nf=1 ad='int((nf+1)/2) * W/nf * 0.29'
+ as='int((nf+2)/2) * W/nf * 0.29' pd='2*int((nf+1)/2) * (W/nf + 0.29)' ps='2*int((nf+2)/2) * (W/nf + 0.29)'
+ nrd='0.29 / W' nrs='0.29 / W' sa=0 sb=0 sd=0 mult=1 m=1
XM107 net30 net22 net31 VDD sky130_fd_pr__pfet_01v8 L={L} W={W/2} nf=1 ad='int((nf+1)/2) * W/nf * 0.29'
+ as='int((nf+2)/2) * W/nf * 0.29' pd='2*int((nf+1)/2) * (W/nf + 0.29)' ps='2*int((nf+2)/2) * (W/nf + 0.29)'
+ nrd='0.29 / W' nrs='0.29 / W' sa=0 sb=0 sd=0 mult=1 m=1
XM108 net31 net22 net32 VDD sky130_fd_pr__pfet_01v8 L={L} W={W/2} nf=1 ad='int((nf+1)/2) * W/nf * 0.29'
+ as='int((nf+2)/2) * W/nf * 0.29' pd='2*int((nf+1)/2) * (W/nf + 0.29)' ps='2*int((nf+2)/2) * (W/nf + 0.29)'
+ nrd='0.29 / W' nrs='0.29 / W' sa=0 sb=0 sd=0 mult=1 m=1
XM109 net32 net22 net23 VDD sky130_fd_pr__pfet_01v8 L={L} W={W/2} nf=1 ad='int((nf+1)/2) * W/nf * 0.29'
+ as='int((nf+2)/2) * W/nf * 0.29' pd='2*int((nf+1)/2) * (W/nf + 0.29)' ps='2*int((nf+2)/2) * (W/nf + 0.29)'
+ nrd='0.29 / W' nrs='0.29 / W' sa=0 sb=0 sd=0 mult=1 m=1
XM111 net23 net22 net28 VDD sky130_fd_pr__pfet_01v8 L={L} W={W/2} nf=1 ad='int((nf+1)/2) * W/nf * 0.29'
+ as='int((nf+2)/2) * W/nf * 0.29' pd='2*int((nf+1)/2) * (W/nf + 0.29)' ps='2*int((nf+2)/2) * (W/nf + 0.29)'
+ nrd='0.29 / W' nrs='0.29 / W' sa=0 sb=0 sd=0 mult=1 m=1
XM114 net28 net22 net27 VDD sky130_fd_pr__pfet_01v8 L={L} W={W/2} nf=1 ad='int((nf+1)/2) * W/nf * 0.29'
+ as='int((nf+2)/2) * W/nf * 0.29' pd='2*int((nf+1)/2) * (W/nf + 0.29)' ps='2*int((nf+2)/2) * (W/nf + 0.29)'
+ nrd='0.29 / W' nrs='0.29 / W' sa=0 sb=0 sd=0 mult=1 m=1
XM115 net27 net22 net26 VDD sky130_fd_pr__pfet_01v8 L={L} W={W/2} nf=1 ad='int((nf+1)/2) * W/nf * 0.29'
+ as='int((nf+2)/2) * W/nf * 0.29' pd='2*int((nf+1)/2) * (W/nf + 0.29)' ps='2*int((nf+2)/2) * (W/nf + 0.29)'
+ nrd='0.29 / W' nrs='0.29 / W' sa=0 sb=0 sd=0 mult=1 m=1
XM116 net26 net22 net25 VDD sky130_fd_pr__pfet_01v8 L={L} W={W/2} nf=1 ad='int((nf+1)/2) * W/nf * 0.29'
+ as='int((nf+2)/2) * W/nf * 0.29' pd='2*int((nf+1)/2) * (W/nf + 0.29)' ps='2*int((nf+2)/2) * (W/nf + 0.29)'
+ nrd='0.29 / W' nrs='0.29 / W' sa=0 sb=0 sd=0 mult=1 m=1
XM117 net24 GND GND GND sky130_fd_pr__nfet_01v8 L={L} W={W/2} nf=1 ad='int((nf+1)/2) * W/nf * 0.29' as='int((nf+2)/2) * W/nf * 0.29'
+ pd='2*int((nf+1)/2) * (W/nf + 0.29)' ps='2*int((nf+2)/2) * (W/nf + 0.29)' nrd='0.29 / W' nrs='0.29 / W'
+ sa=0 sb=0 sd=0 mult=1 m=1
XM118 net21 net21 net24 GND sky130_fd_pr__nfet_01v8 L={L} W={W/2} nf=1 ad='int((nf+1)/2) * W/nf * 0.29'
+ as='int((nf+2)/2) * W/nf * 0.29' pd='2*int((nf+1)/2) * (W/nf + 0.29)' ps='2*int((nf+2)/2) * (W/nf + 0.29)'
+ nrd='0.29 / W' nrs='0.29 / W' sa=0 sb=0 sd=0 mult=1 m=1
XM119 net46 net21 net21 GND sky130_fd_pr__nfet_01v8 L={L} W={W/2} nf=1 ad='int((nf+1)/2) * W/nf * 0.29'
+ as='int((nf+2)/2) * W/nf * 0.29' pd='2*int((nf+1)/2) * (W/nf + 0.29)' ps='2*int((nf+2)/2) * (W/nf + 0.29)'
+ nrd='0.29 / W' nrs='0.29 / W' sa=0 sb=0 sd=0 mult=1 m=1
XM122 GND GND net8 GND sky130_fd_pr__nfet_01v8 L={L} W={W/2} nf=1 ad='int((nf+1)/2) * W/nf * 0.29' as='int((nf+2)/2) * W/nf * 0.29'
+ pd='2*int((nf+1)/2) * (W/nf + 0.29)' ps='2*int((nf+2)/2) * (W/nf + 0.29)' nrd='0.29 / W' nrs='0.29 / W'
+ sa=0 sb=0 sd=0 mult=1 m=1
X7 GND Vbn b0out b0 mux
X9 GND Vbn b1out b1 mux
X10 GND Vbn net43 b2 mux
X11 GND Vbn net45 b3 mux
X12 GND Vbn net44 b4 mux
X13 GND Vbn net42 b5 mux
X14 GND Vbn b6out b6 mux
Vout1 net10 net40 0
.save i(vout1)
XM123 net34 net21 net33 GND sky130_fd_pr__nfet_01v8 L={L} W={W} nf=1 ad='int((nf+1)/2) * W/nf * 0.29'
+ as='int((nf+2)/2) * W/nf * 0.29' pd='2*int((nf+1)/2) * (W/nf + 0.29)' ps='2*int((nf+2)/2) * (W/nf + 0.29)'
+ nrd='0.29 / W' nrs='0.29 / W' sa=0 sb=0 sd=0 mult=1 m=1
XM124 net33 net21 net34 GND sky130_fd_pr__nfet_01v8 L={L} W={W} nf=1 ad='int((nf+1)/2) * W/nf * 0.29'
+ as='int((nf+2)/2) * W/nf * 0.29' pd='2*int((nf+1)/2) * (W/nf + 0.29)' ps='2*int((nf+2)/2) * (W/nf + 0.29)'
+ nrd='0.29 / W' nrs='0.29 / W' sa=0 sb=0 sd=0 mult=1 m=1
XM125 net34 net21 net35 GND sky130_fd_pr__nfet_01v8 L={L} W={W} nf=1 ad='int((nf+1)/2) * W/nf * 0.29'
+ as='int((nf+2)/2) * W/nf * 0.29' pd='2*int((nf+1)/2) * (W/nf + 0.29)' ps='2*int((nf+2)/2) * (W/nf + 0.29)'
+ nrd='0.29 / W' nrs='0.29 / W' sa=0 sb=0 sd=0 mult=1 m=1
XM126 net35 net21 net34 GND sky130_fd_pr__nfet_01v8 L={L} W={W} nf=1 ad='int((nf+1)/2) * W/nf * 0.29'
+ as='int((nf+2)/2) * W/nf * 0.29' pd='2*int((nf+1)/2) * (W/nf + 0.29)' ps='2*int((nf+2)/2) * (W/nf + 0.29)'
+ nrd='0.29 / W' nrs='0.29 / W' sa=0 sb=0 sd=0 mult=1 m=1
XM127 GND b0out net34 GND sky130_fd_pr__nfet_01v8 L={L} W={W} nf=1 ad='int((nf+1)/2) * W/nf * 0.29' as='int((nf+2)/2) * W/nf * 0.29'
+ pd='2*int((nf+1)/2) * (W/nf + 0.29)' ps='2*int((nf+2)/2) * (W/nf + 0.29)' nrd='0.29 / W' nrs='0.29 / W'
+ sa=0 sb=0 sd=0 mult=1 m=1
XM128 net33 b1out GND GND sky130_fd_pr__nfet_01v8 L={L} W={W} nf=1 ad='int((nf+1)/2) * W/nf * 0.29' as='int((nf+2)/2) * W/nf * 0.29'
+ pd='2*int((nf+1)/2) * (W/nf + 0.29)' ps='2*int((nf+2)/2) * (W/nf + 0.29)' nrd='0.29 / W' nrs='0.29 / W'
+ sa=0 sb=0 sd=0 mult=1 m=1
XM129 GND net42 net36 GND sky130_fd_pr__nfet_01v8 L={L} W={W} nf=1 ad='int((nf+1)/2) * W/nf * 0.29' as='int((nf+2)/2) * W/nf * 0.29'
+ pd='2*int((nf+1)/2) * (W/nf + 0.29)' ps='2*int((nf+2)/2) * (W/nf + 0.29)' nrd='0.29 / W' nrs='0.29 / W'
+ sa=0 sb=0 sd=0 mult=1 m=1
XM130 net33 net21 net37 GND sky130_fd_pr__nfet_01v8 L={L} W={W} nf=1 ad='int((nf+1)/2) * W/nf * 0.29'
+ as='int((nf+2)/2) * W/nf * 0.29' pd='2*int((nf+1)/2) * (W/nf + 0.29)' ps='2*int((nf+2)/2) * (W/nf + 0.29)'
+ nrd='0.29 / W' nrs='0.29 / W' sa=0 sb=0 sd=0 mult=1 m=1
XM131 net37 net21 net33 GND sky130_fd_pr__nfet_01v8 L={L} W={W} nf=1 ad='int((nf+1)/2) * W/nf * 0.29'
+ as='int((nf+2)/2) * W/nf * 0.29' pd='2*int((nf+1)/2) * (W/nf + 0.29)' ps='2*int((nf+2)/2) * (W/nf + 0.29)'
+ nrd='0.29 / W' nrs='0.29 / W' sa=0 sb=0 sd=0 mult=1 m=1
XM132 net33 net21 net35 GND sky130_fd_pr__nfet_01v8 L={L} W={W} nf=1 ad='int((nf+1)/2) * W/nf * 0.29'
+ as='int((nf+2)/2) * W/nf * 0.29' pd='2*int((nf+1)/2) * (W/nf + 0.29)' ps='2*int((nf+2)/2) * (W/nf + 0.29)'
+ nrd='0.29 / W' nrs='0.29 / W' sa=0 sb=0 sd=0 mult=1 m=1
XM133 net35 net21 net37 GND sky130_fd_pr__nfet_01v8 L={L} W={W} nf=1 ad='int((nf+1)/2) * W/nf * 0.29'
+ as='int((nf+2)/2) * W/nf * 0.29' pd='2*int((nf+1)/2) * (W/nf + 0.29)' ps='2*int((nf+2)/2) * (W/nf + 0.29)'
+ nrd='0.29 / W' nrs='0.29 / W' sa=0 sb=0 sd=0 mult=1 m=1
XM134 net37 net21 net38 GND sky130_fd_pr__nfet_01v8 L={L} W={W} nf=1 ad='int((nf+1)/2) * W/nf * 0.29'
+ as='int((nf+2)/2) * W/nf * 0.29' pd='2*int((nf+1)/2) * (W/nf + 0.29)' ps='2*int((nf+2)/2) * (W/nf + 0.29)'
+ nrd='0.29 / W' nrs='0.29 / W' sa=0 sb=0 sd=0 mult=1 m=1
XM135 net38 net21 net37 GND sky130_fd_pr__nfet_01v8 L={L} W={W} nf=1 ad='int((nf+1)/2) * W/nf * 0.29'
+ as='int((nf+2)/2) * W/nf * 0.29' pd='2*int((nf+1)/2) * (W/nf + 0.29)' ps='2*int((nf+2)/2) * (W/nf + 0.29)'
+ nrd='0.29 / W' nrs='0.29 / W' sa=0 sb=0 sd=0 mult=1 m=1
XM136 GND net43 net37 GND sky130_fd_pr__nfet_01v8 L={L} W={W} nf=1 ad='int((nf+1)/2) * W/nf * 0.29' as='int((nf+2)/2) * W/nf * 0.29'
+ pd='2*int((nf+1)/2) * (W/nf + 0.29)' ps='2*int((nf+2)/2) * (W/nf + 0.29)' nrd='0.29 / W' nrs='0.29 / W'
+ sa=0 sb=0 sd=0 mult=1 m=1
XM137 net39 net21 net36 GND sky130_fd_pr__nfet_01v8 L={L} W={W} nf=1 ad='int((nf+1)/2) * W/nf * 0.29'
+ as='int((nf+2)/2) * W/nf * 0.29' pd='2*int((nf+1)/2) * (W/nf + 0.29)' ps='2*int((nf+2)/2) * (W/nf + 0.29)'
+ nrd='0.29 / W' nrs='0.29 / W' sa=0 sb=0 sd=0 mult=1 m=1
XM138 net36 net21 net39 GND sky130_fd_pr__nfet_01v8 L={L} W={W} nf=1 ad='int((nf+1)/2) * W/nf * 0.29'
+ as='int((nf+2)/2) * W/nf * 0.29' pd='2*int((nf+1)/2) * (W/nf + 0.29)' ps='2*int((nf+2)/2) * (W/nf + 0.29)'
+ nrd='0.29 / W' nrs='0.29 / W' sa=0 sb=0 sd=0 mult=1 m=1
XM139 net35 net21 net36 GND sky130_fd_pr__nfet_01v8 L={L} W={W} nf=1 ad='int((nf+1)/2) * W/nf * 0.29'
+ as='int((nf+2)/2) * W/nf * 0.29' pd='2*int((nf+1)/2) * (W/nf + 0.29)' ps='2*int((nf+2)/2) * (W/nf + 0.29)'
+ nrd='0.29 / W' nrs='0.29 / W' sa=0 sb=0 sd=0 mult=1 m=1
XM140 net39 net21 net35 GND sky130_fd_pr__nfet_01v8 L={L} W={W} nf=1 ad='int((nf+1)/2) * W/nf * 0.29'
+ as='int((nf+2)/2) * W/nf * 0.29' pd='2*int((nf+1)/2) * (W/nf + 0.29)' ps='2*int((nf+2)/2) * (W/nf + 0.29)'
+ nrd='0.29 / W' nrs='0.29 / W' sa=0 sb=0 sd=0 mult=1 m=1
XM141 net38 net21 net39 GND sky130_fd_pr__nfet_01v8 L={L} W={W} nf=1 ad='int((nf+1)/2) * W/nf * 0.29'
+ as='int((nf+2)/2) * W/nf * 0.29' pd='2*int((nf+1)/2) * (W/nf + 0.29)' ps='2*int((nf+2)/2) * (W/nf + 0.29)'
+ nrd='0.29 / W' nrs='0.29 / W' sa=0 sb=0 sd=0 mult=1 m=1
XM142 net39 net21 net38 GND sky130_fd_pr__nfet_01v8 L={L} W={W} nf=1 ad='int((nf+1)/2) * W/nf * 0.29'
+ as='int((nf+2)/2) * W/nf * 0.29' pd='2*int((nf+1)/2) * (W/nf + 0.29)' ps='2*int((nf+2)/2) * (W/nf + 0.29)'
+ nrd='0.29 / W' nrs='0.29 / W' sa=0 sb=0 sd=0 mult=1 m=1
XM143 net39 net44 GND GND sky130_fd_pr__nfet_01v8 L={L} W={W} nf=1 ad='int((nf+1)/2) * W/nf * 0.29' as='int((nf+2)/2) * W/nf * 0.29'
+ pd='2*int((nf+1)/2) * (W/nf + 0.29)' ps='2*int((nf+2)/2) * (W/nf + 0.29)' nrd='0.29 / W' nrs='0.29 / W'
+ sa=0 sb=0 sd=0 mult=1 m=1
XM144 net40 net21 net41 GND sky130_fd_pr__nfet_01v8 L={L} W={W} nf=1 ad='int((nf+1)/2) * W/nf * 0.29'
+ as='int((nf+2)/2) * W/nf * 0.29' pd='2*int((nf+1)/2) * (W/nf + 0.29)' ps='2*int((nf+2)/2) * (W/nf + 0.29)'
+ nrd='0.29 / W' nrs='0.29 / W' sa=0 sb=0 sd=0 mult=1 m=1
XM145 net41 net21 net40 GND sky130_fd_pr__nfet_01v8 L={L} W={W} nf=1 ad='int((nf+1)/2) * W/nf * 0.29'
+ as='int((nf+2)/2) * W/nf * 0.29' pd='2*int((nf+1)/2) * (W/nf + 0.29)' ps='2*int((nf+2)/2) * (W/nf + 0.29)'
+ nrd='0.29 / W' nrs='0.29 / W' sa=0 sb=0 sd=0 mult=1 m=1
XM146 net36 net21 net41 GND sky130_fd_pr__nfet_01v8 L={L} W={W} nf=1 ad='int((nf+1)/2) * W/nf * 0.29'
+ as='int((nf+2)/2) * W/nf * 0.29' pd='2*int((nf+1)/2) * (W/nf + 0.29)' ps='2*int((nf+2)/2) * (W/nf + 0.29)'
+ nrd='0.29 / W' nrs='0.29 / W' sa=0 sb=0 sd=0 mult=1 m=1
XM147 net41 net21 net36 GND sky130_fd_pr__nfet_01v8 L={L} W={W} nf=1 ad='int((nf+1)/2) * W/nf * 0.29'
+ as='int((nf+2)/2) * W/nf * 0.29' pd='2*int((nf+1)/2) * (W/nf + 0.29)' ps='2*int((nf+2)/2) * (W/nf + 0.29)'
+ nrd='0.29 / W' nrs='0.29 / W' sa=0 sb=0 sd=0 mult=1 m=1
XM148 net41 b6out GND GND sky130_fd_pr__nfet_01v8 L={L} W={W} nf=1 ad='int((nf+1)/2) * W/nf * 0.29' as='int((nf+2)/2) * W/nf * 0.29'
+ pd='2*int((nf+1)/2) * (W/nf + 0.29)' ps='2*int((nf+2)/2) * (W/nf + 0.29)' nrd='0.29 / W' nrs='0.29 / W'
+ sa=0 sb=0 sd=0 mult=1 m=1
XM149 GND net45 net38 GND sky130_fd_pr__nfet_01v8 L={L} W={W} nf=1 ad='int((nf+1)/2) * W/nf * 0.29' as='int((nf+2)/2) * W/nf * 0.29'
+ pd='2*int((nf+1)/2) * (W/nf + 0.29)' ps='2*int((nf+2)/2) * (W/nf + 0.29)' nrd='0.29 / W' nrs='0.29 / W'
+ sa=0 sb=0 sd=0 mult=1 m=1
XM150 net35 net21 net38 GND sky130_fd_pr__nfet_01v8 L={L} W={W} nf=1 ad='int((nf+1)/2) * W/nf * 0.29'
+ as='int((nf+2)/2) * W/nf * 0.29' pd='2*int((nf+1)/2) * (W/nf + 0.29)' ps='2*int((nf+2)/2) * (W/nf + 0.29)'
+ nrd='0.29 / W' nrs='0.29 / W' sa=0 sb=0 sd=0 mult=1 m=1
XM151 VDD net35 net35 VDD sky130_fd_pr__pfet_01v8 L={L} W={W} nf=1 ad='int((nf+1)/2) * W/nf * 0.29' as='int((nf+2)/2) * W/nf * 0.29'
+ pd='2*int((nf+1)/2) * (W/nf + 0.29)' ps='2*int((nf+2)/2) * (W/nf + 0.29)' nrd='0.29 / W' nrs='0.29 / W'
+ sa=0 sb=0 sd=0 mult=1 m=1
**** begin user architecture code

.param W=24
.param L=1
.control
set wr_vecnames
set wr_singlescale
let code = 0
  while code < 128
    if code eq 0
      let b0 = 0
    else
      let b0 = code % 2 * 1.8
    end
    if floor(code / 2) eq 0
      let b1 = 0
    else
      let b1 = floor(code / 2) % 2 * 1.8
    end
    if floor(code / 4) eq 0
      let b2 = 0
    else
      let b2 = floor(code / 4) % 2 * 1.8
    end
    if floor(code / 8) eq 0
      let b3 = 0
    else
      let b3 = floor(code / 8) % 2 * 1.8
    end
    if floor(code / 16) eq 0
      let b4 = 0
    else
      let b4 = floor(code / 16) % 2 * 1.8
    end
    if floor(code / 32) eq 0
      let b5 = 0
    else
      let b5 = floor(code / 32) % 2 * 1.8
    end
    if floor(code / 64) eq 0
      let b6 = 0
    else
      let b6 = floor(code / 64) % 2 * 1.8
    end
    alter v0 $&b0
    alter v1 $&b1
    alter v2 $&b2
    alter v3 $&b3
    alter v4 $&b4
    alter v5 $&b5
    alter v6 $&b6
    save all
    op
    wrdata ~/Documents/current-output-dac-vlsi/simulations/dac_sim.txt v(Vbn) i(Vout) i(Vout1) v(b6)
+ v(b5) v(b4) v(b3) v(b2) v(b1) v(b0) v(b0out) v(b1out) v(b6out)
    if code eq 0
      set appendwrite
      set wr_vecnames = FALSE
    end
    let code = code + 1
  end
.endc


.option wnflag=1
.param MC_SWITCH=0.0
.lib ~/skywater/skywater-pdk/libraries/sky130_fd_pr_ngspice/latest/models/sky130.lib.spice tt

**** end user architecture code
**.ends

* expanding   symbol:  /home/madvlsi/Documents/current-output-dac-vlsi/schematics/mux.sym # of
*+ pins=4
** sym_path: /home/madvlsi/Documents/current-output-dac-vlsi/schematics/mux.sym
** sch_path: /home/madvlsi/Documents/current-output-dac-vlsi/schematics/mux.sch
.subckt mux A B Y S
*.ipin S
*.ipin A
*.opin Y
*.ipin B
XM1 net1 S GND GND sky130_fd_pr__nfet_01v8 L=0.15 W=1 nf=1 ad='int((nf+1)/2) * W/nf * 0.29' as='int((nf+2)/2) * W/nf * 0.29'
+ pd='2*int((nf+1)/2) * (W/nf + 0.29)' ps='2*int((nf+2)/2) * (W/nf + 0.29)' nrd='0.29 / W' nrs='0.29 / W'
+ sa=0 sb=0 sd=0 mult=1 m=1
XM2 net1 S VDD VDD sky130_fd_pr__pfet_01v8 L=0.15 W=1 nf=1 ad='int((nf+1)/2) * W/nf * 0.29' as='int((nf+2)/2) * W/nf * 0.29'
+ pd='2*int((nf+1)/2) * (W/nf + 0.29)' ps='2*int((nf+2)/2) * (W/nf + 0.29)' nrd='0.29 / W' nrs='0.29 / W'
+ sa=0 sb=0 sd=0 mult=1 m=1
XM3 Y S B GND sky130_fd_pr__nfet_01v8 L=0.15 W=1 nf=1 ad='int((nf+1)/2) * W/nf * 0.29' as='int((nf+2)/2) * W/nf * 0.29'
+ pd='2*int((nf+1)/2) * (W/nf + 0.29)' ps='2*int((nf+2)/2) * (W/nf + 0.29)' nrd='0.29 / W' nrs='0.29 / W'
+ sa=0 sb=0 sd=0 mult=1 m=1
XM4 A net1 Y GND sky130_fd_pr__nfet_01v8 L=0.15 W=1 nf=1 ad='int((nf+1)/2) * W/nf * 0.29' as='int((nf+2)/2) * W/nf * 0.29'
+ pd='2*int((nf+1)/2) * (W/nf + 0.29)' ps='2*int((nf+2)/2) * (W/nf + 0.29)' nrd='0.29 / W' nrs='0.29 / W'
+ sa=0 sb=0 sd=0 mult=1 m=1
.ends

.GLOBAL GND
.GLOBAL VDD
.end
